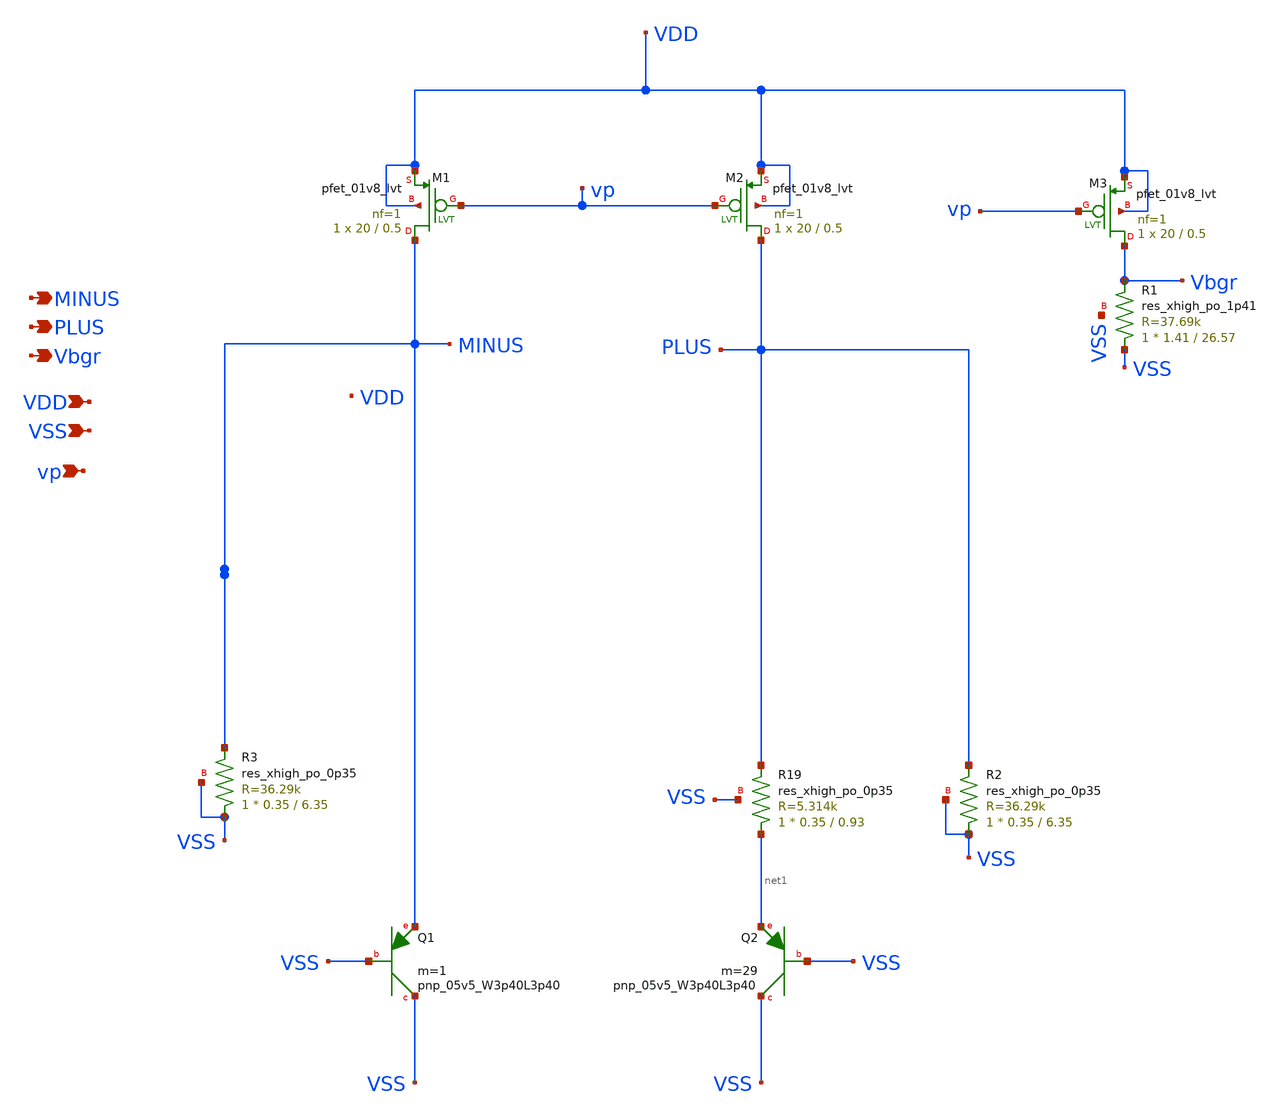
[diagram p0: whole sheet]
** sch_path: xschem/core_PreL.sch
**.subckt core_PreL MINUS PLUS Vbgr VDD VSS vp
*.opin MINUS
*.opin PLUS
*.opin Vbgr
*.ipin VDD
*.ipin VSS
*.ipin vp
XQ1 VSS VSS MINUS sky130_fd_pr__pnp_05v5_W3p40L3p40 m=1
XQ2 VSS VSS net1 sky130_fd_pr__pnp_05v5_W3p40L3p40 m=29
XM1 MINUS vp VDD VDD sky130_fd_pr__pfet_01v8_lvt L=0.5 W=20 nf=1 ad='int((nf+1)/2) * W/nf * 0.29' as='int((nf+2)/2) * W/nf * 0.29'
+ pd='2*int((nf+1)/2) * (W/nf + 0.29)' ps='2*int((nf+2)/2) * (W/nf + 0.29)' nrd='0.29 / W' nrs='0.29 / W'
+ sa=0 sb=0 sd=0 mult=1 m=1
XM2 PLUS vp VDD VDD sky130_fd_pr__pfet_01v8_lvt L=0.5 W=20 nf=1 ad='int((nf+1)/2) * W/nf * 0.29' as='int((nf+2)/2) * W/nf * 0.29'
+ pd='2*int((nf+1)/2) * (W/nf + 0.29)' ps='2*int((nf+2)/2) * (W/nf + 0.29)' nrd='0.29 / W' nrs='0.29 / W'
+ sa=0 sb=0 sd=0 mult=1 m=1
XM3 Vbgr vp VDD VDD sky130_fd_pr__pfet_01v8_lvt L=0.5 W=20 nf=1 ad='int((nf+1)/2) * W/nf * 0.29' as='int((nf+2)/2) * W/nf * 0.29'
+ pd='2*int((nf+1)/2) * (W/nf + 0.29)' ps='2*int((nf+2)/2) * (W/nf + 0.29)' nrd='0.29 / W' nrs='0.29 / W'
+ sa=0 sb=0 sd=0 mult=1 m=1
XR19 net1 PLUS VSS sky130_fd_pr__res_xhigh_po_0p35 L=0.93 mult=1 m=1
XR2 VSS PLUS VSS sky130_fd_pr__res_xhigh_po_0p35 L=6.35 mult=1 m=1
XR3 VSS MINUS VSS sky130_fd_pr__res_xhigh_po_0p35 L=6.35 mult=1 m=1
XR1 VSS Vbgr VSS sky130_fd_pr__res_xhigh_po_1p41 L=26.57 mult=1 m=1
**.ends
.end
